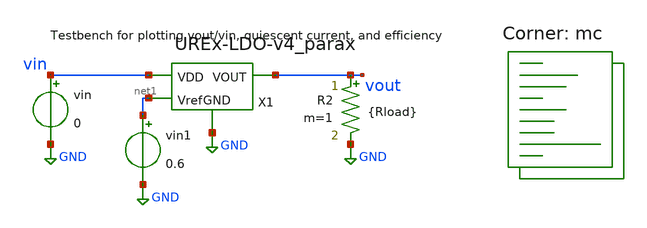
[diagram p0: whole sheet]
** sch_path: xschem/corner-sims/VoutvsVin-v4-cornersim.sch
**.subckt VoutvsVin-v4-cornersim
vin vin GND 0
R2 vout GND {Rload} m=1
X1 vin vout GND net1 UREx-LDO-v4_parax
vin1 net1 GND 0.6
**** begin user architecture code


.param mc_mm_switch=1
.param mc_pr_switch=1
.param Rload=20
.control
  dc vin 0.5 5 0.1
  wrdata mc_out.csv v(vin) v(vout)

  set appendwrite

  repeat 100
    reset
    dc vin 0.5 5 0.1
    wrdata mc_out.csv v(vin) v(vout)
  end
.endc


.lib $::SKYWATER_MODELS/sky130.lib.spice mc
**** end user architecture code
**.ends

* expanding   symbol:  UREx-LDO-v4_parax.sym # of pins=4
** sym_path: xschem/UREx-LDO-v4.sym
.include [file normalize UREx-LDO-v4_parax.spice]
.GLOBAL GND
.end
